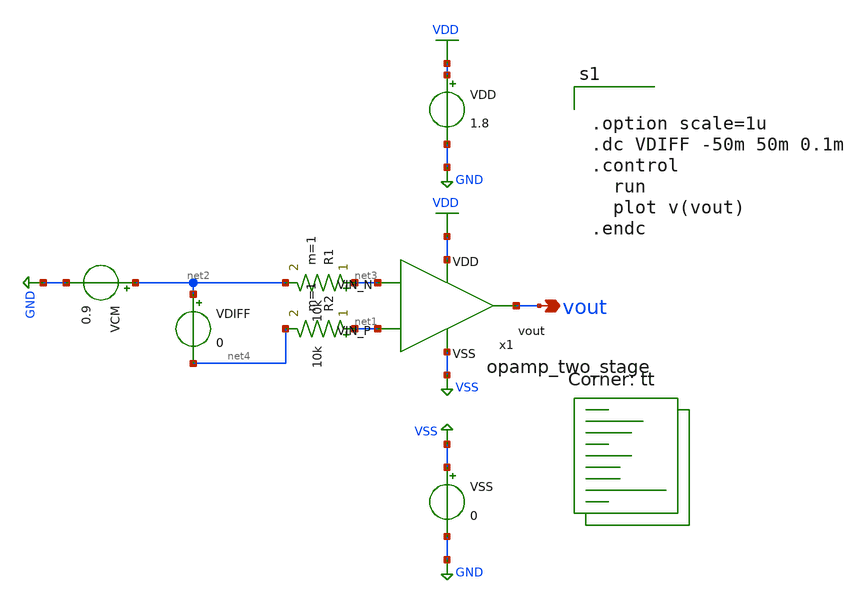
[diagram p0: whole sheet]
** sch_path: analog/schematics/tb_dc_analysis.sch
**.subckt tb_dc_analysis vout
*.opin vout
VDD VDD GND 1.8
VSS VSS GND 0
VCM net2 GND 0.9
VDIFF net2 net4 0
x1 VDD vout net1 net3 VSS opamp_two_stage
R1 net3 net2 10k m=1
R2 net1 net4 10k m=1
**** begin user architecture code


.option scale=1u
.dc VDIFF -50m 50m 0.1m
.control
  run
  plot v(vout)
.endc


.lib $::SKYWATER_MODELS/sky130.lib.spice tt
**** end user architecture code
**.ends

* expanding   symbol:  opamp_two_stage.sym # of pins=5
** sym_path: analog/schematics/opamp_two_stage.sym
** sch_path: analog/schematics/opamp_two_stage.sch
.subckt opamp_two_stage VDD vout VIN_P VIN_N VSS
*.ipin VIN_P
*.ipin VIN_N
*.opin vout
*.ipin VDD
*.ipin VSS
XM1 net3 VIN_N net4 VSS sky130_fd_pr__nfet_01v8 L=0.5 W=0.42 nf=1 ad='int((nf+1)/2) * W/nf * 0.29' as='int((nf+2)/2) * W/nf * 0.29'
+ pd='2*int((nf+1)/2) * (W/nf + 0.29)' ps='2*int((nf+2)/2) * (W/nf + 0.29)' nrd='0.29 / W' nrs='0.29 / W'
+ sa=0 sb=0 sd=0 mult=1 m=1
XM2 net5 VIN_P net4 VSS sky130_fd_pr__nfet_01v8 L=0.5 W=0.42 nf=1 ad='int((nf+1)/2) * W/nf * 0.29' as='int((nf+2)/2) * W/nf * 0.29'
+ pd='2*int((nf+1)/2) * (W/nf + 0.29)' ps='2*int((nf+2)/2) * (W/nf + 0.29)' nrd='0.29 / W' nrs='0.29 / W'
+ sa=0 sb=0 sd=0 mult=1 m=1
XM3 net3 net5 VDD VDD sky130_fd_pr__pfet_01v8 L=0.5 W=0.42 nf=1 ad='int((nf+1)/2) * W/nf * 0.29' as='int((nf+2)/2) * W/nf * 0.29'
+ pd='2*int((nf+1)/2) * (W/nf + 0.29)' ps='2*int((nf+2)/2) * (W/nf + 0.29)' nrd='0.29 / W' nrs='0.29 / W'
+ sa=0 sb=0 sd=0 mult=1 m=1
XM4 net5 net5 VDD VDD sky130_fd_pr__pfet_01v8 L=0.5 W=0.42 nf=1 ad='int((nf+1)/2) * W/nf * 0.29' as='int((nf+2)/2) * W/nf * 0.29'
+ pd='2*int((nf+1)/2) * (W/nf + 0.29)' ps='2*int((nf+2)/2) * (W/nf + 0.29)' nrd='0.29 / W' nrs='0.29 / W'
+ sa=0 sb=0 sd=0 mult=1 m=1
XM5 vout net3 VDD VDD sky130_fd_pr__pfet_01v8 L=0.5 W=2 nf=1 ad='int((nf+1)/2) * W/nf * 0.29' as='int((nf+2)/2) * W/nf * 0.29'
+ pd='2*int((nf+1)/2) * (W/nf + 0.29)' ps='2*int((nf+2)/2) * (W/nf + 0.29)' nrd='0.29 / W' nrs='0.29 / W'
+ sa=0 sb=0 sd=0 mult=2 m=2
XM6 vout net1 VSS VSS sky130_fd_pr__nfet_01v8 L=0.5 W=0.42 nf=1 ad='int((nf+1)/2) * W/nf * 0.29' as='int((nf+2)/2) * W/nf * 0.29'
+ pd='2*int((nf+1)/2) * (W/nf + 0.29)' ps='2*int((nf+2)/2) * (W/nf + 0.29)' nrd='0.29 / W' nrs='0.29 / W'
+ sa=0 sb=0 sd=0 mult=2 m=2
XM7 net4 net1 VSS VSS sky130_fd_pr__nfet_01v8 L=0.5 W=0.42 nf=1 ad='int((nf+1)/2) * W/nf * 0.29' as='int((nf+2)/2) * W/nf * 0.29'
+ pd='2*int((nf+1)/2) * (W/nf + 0.29)' ps='2*int((nf+2)/2) * (W/nf + 0.29)' nrd='0.29 / W' nrs='0.29 / W'
+ sa=0 sb=0 sd=0 mult=2 m=2
XR1 net3 net2 VSS sky130_fd_pr__res_high_po W=1 L=1 mult=1 m=1
XC1 vout net2 sky130_fd_pr__cap_mim_m3_1 W=1 L=1 MF=1 m=1
XR2 net1 VDD VSS sky130_fd_pr__res_high_po W=1 L=1 mult=1 m=1
.ends

.GLOBAL VDD
.GLOBAL GND
.GLOBAL VSS
.end
